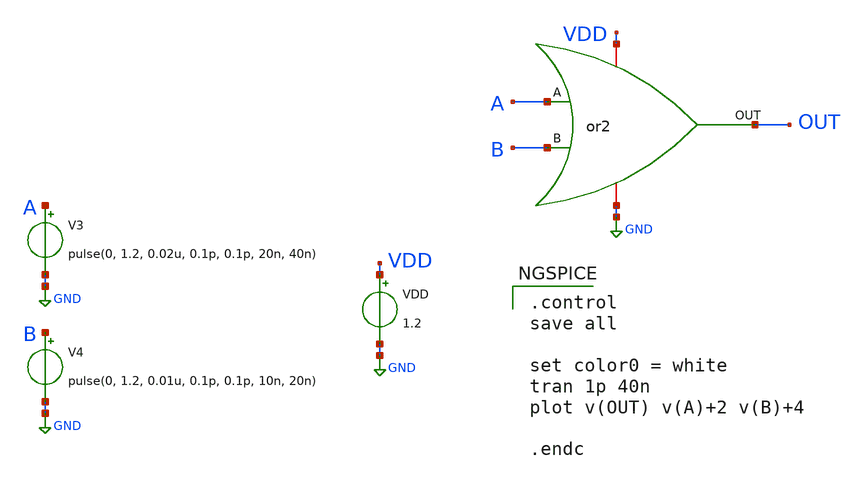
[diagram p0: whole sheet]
** sch_path: design/ALU/or2_tb.sch
**.subckt or2_tb
VDD VDD GND 1.2
V3 A GND pulse(0, 1.2, 0.02u, 0.1p, 0.1p, 20n, 40n)
V4 B GND pulse(0, 1.2, 0.01u, 0.1p, 0.1p, 10n, 20n)
x1 A B GND VDD OUT or2
**** begin user architecture code

** opencircuitdesign pdks install
.lib $::SKYWATER_MODELS/sky130.lib.spice tt_mm



.control
save all

set color0 = white
tran 1p 40n
plot v(OUT) v(A)+2 v(B)+4

.endc

**** end user architecture code
**.ends

* expanding   symbol:  or2.sym # of pins=5
** sym_path: design/8_BIT_OR/xschem/or2.sym
** sch_path: design/8_BIT_OR/xschem/or2.sch
.subckt or2 A B VSS VDD OUT
*.ipin A
*.ipin B
*.iopin VSS
*.iopin VDD
*.opin OUT
XM3 net1 A net2 VDD sky130_fd_pr__pfet_01v8 L=0.15 W=6.4 nf=1 ad='int((nf+1)/2) * W/nf * 0.29' as='int((nf+2)/2) * W/nf * 0.29'
+ pd='2*int((nf+1)/2) * (W/nf + 0.29)' ps='2*int((nf+2)/2) * (W/nf + 0.29)' nrd='0.29 / W' nrs='0.29 / W'
+ sa=0 sb=0 sd=0 mult=1 m=1
XM4 net2 B VDD VDD sky130_fd_pr__pfet_01v8 L=0.15 W=6.4 nf=1 ad='int((nf+1)/2) * W/nf * 0.29' as='int((nf+2)/2) * W/nf * 0.29'
+ pd='2*int((nf+1)/2) * (W/nf + 0.29)' ps='2*int((nf+2)/2) * (W/nf + 0.29)' nrd='0.29 / W' nrs='0.29 / W'
+ sa=0 sb=0 sd=0 mult=1 m=1
XM1 net1 A VSS VSS sky130_fd_pr__nfet_01v8 L=0.15 W=1 nf=1 ad='int((nf+1)/2) * W/nf * 0.29' as='int((nf+2)/2) * W/nf * 0.29'
+ pd='2*int((nf+1)/2) * (W/nf + 0.29)' ps='2*int((nf+2)/2) * (W/nf + 0.29)' nrd='0.29 / W' nrs='0.29 / W'
+ sa=0 sb=0 sd=0 mult=1 m=1
XM2 net1 B VSS VSS sky130_fd_pr__nfet_01v8 L=0.15 W=1 nf=1 ad='int((nf+1)/2) * W/nf * 0.29' as='int((nf+2)/2) * W/nf * 0.29'
+ pd='2*int((nf+1)/2) * (W/nf + 0.29)' ps='2*int((nf+2)/2) * (W/nf + 0.29)' nrd='0.29 / W' nrs='0.29 / W'
+ sa=0 sb=0 sd=0 mult=1 m=1
XM5 OUT net1 VDD VDD sky130_fd_pr__pfet_01v8 L=0.15 W=6.4 nf=1 ad='int((nf+1)/2) * W/nf * 0.29' as='int((nf+2)/2) * W/nf * 0.29'
+ pd='2*int((nf+1)/2) * (W/nf + 0.29)' ps='2*int((nf+2)/2) * (W/nf + 0.29)' nrd='0.29 / W' nrs='0.29 / W'
+ sa=0 sb=0 sd=0 mult=1 m=1
XM6 OUT net1 VSS VSS sky130_fd_pr__nfet_01v8 L=0.15 W=1 nf=1 ad='int((nf+1)/2) * W/nf * 0.29' as='int((nf+2)/2) * W/nf * 0.29'
+ pd='2*int((nf+1)/2) * (W/nf + 0.29)' ps='2*int((nf+2)/2) * (W/nf + 0.29)' nrd='0.29 / W' nrs='0.29 / W'
+ sa=0 sb=0 sd=0 mult=1 m=1
.ends

.GLOBAL GND
.end
